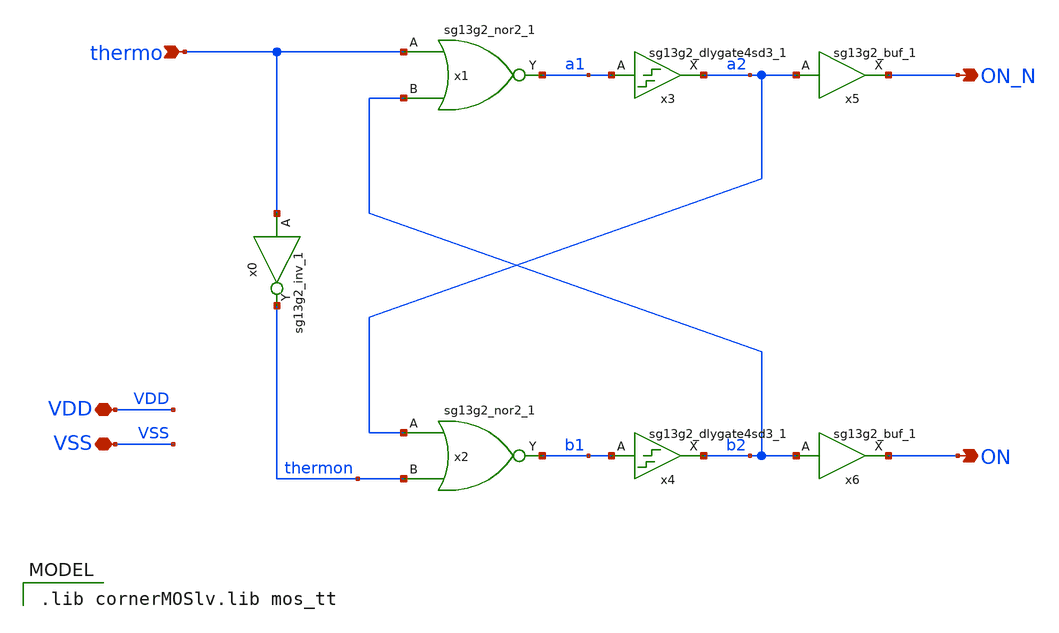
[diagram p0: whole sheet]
** sch_path: analog/non_overlap/xschem/non_overlap.sch
* IHP-GmbH/IHP-Open-PDK/ihp-sg13g2/libs.tech/xschem/sg13g2_stdcells/sg13g2_buf_1.sch:
* Copyright 2023 IHP PDK Authors
* Licensed under the Apache License, Version 2.0 (the "License");
**.subckt non_overlap VSS thermo ON ON_N VDD
*.iopin VSS
*.ipin thermo
*.opin ON
*.opin ON_N
*.iopin VDD
x0 thermon thermo VDD VSS sg13g2_inv_1
x1 a1 thermo b2 VDD VSS sg13g2_nor2_1
x2 b1 a2 thermon VDD VSS sg13g2_nor2_1
x3 a2 a1 VDD VSS sg13g2_dlygate4sd3_1
x4 b2 b1 VDD VSS sg13g2_dlygate4sd3_1
x5 ON_N a2 VDD VSS sg13g2_buf_1
x6 ON b2 VDD VSS sg13g2_buf_1
**** begin user architecture code
 .lib cornerMOSlv.lib mos_tt

**** end user architecture code
**.ends

* expanding   symbol:  sg13g2_stdcells/sg13g2_inv_1.sym # of pins=2
** sym_path: sg13g2_stdcells/sg13g2_inv_1.sym
** sch_path: sg13g2_stdcells/sg13g2_inv_1.sch
.subckt sg13g2_inv_1 Y A VDD VSS
*.opin Y
*.ipin A
*.iopin VDD
*.iopin VSS
XM1 Y A VSS VSS sg13_lv_nmos w=740.00n l=130.00n ng=1 m=1 mm_ok=1
XM2 Y A VDD VDD sg13_lv_pmos w=1.12u l=130.00n ng=1 m=1 mm_ok=1
.ends


* expanding   symbol:  sg13g2_stdcells/sg13g2_nor2_1.sym # of pins=3
** sym_path: sg13g2_stdcells/sg13g2_nor2_1.sym
** sch_path: sg13g2_stdcells/sg13g2_nor2_1.sch
.subckt sg13g2_nor2_1 Y A B VDD VSS
*.opin Y
*.ipin B
*.ipin A
*.iopin VDD
*.iopin VSS
XM1 Y A VSS VSS sg13_lv_nmos w=740.00n l=130.00n ng=1 m=1 mm_ok=1
XM2 Y B VSS VSS sg13_lv_nmos w=740.00n l=130.00n ng=1 m=1 mm_ok=1
XM3 net1 A VDD VDD sg13_lv_pmos w=1.12u l=130.00n ng=1 m=1 mm_ok=1
XM4 Y B net1 VDD sg13_lv_pmos w=1.12u l=130.00n ng=1 m=1 mm_ok=1
.ends


* expanding   symbol:  sg13g2_stdcells/sg13g2_dlygate4sd3_1.sym # of pins=2
** sym_path: sg13g2_stdcells/sg13g2_dlygate4sd3_1.sym
** sch_path: sg13g2_stdcells/sg13g2_dlygate4sd3_1.sch
.subckt sg13g2_dlygate4sd3_1 X A VDD VSS
*.ipin A
*.opin X
*.iopin VDD
*.iopin VSS
XM1 net3 A VSS VSS sg13_lv_nmos w=420.00n l=130.00n ng=1 m=1 mm_ok=1
XM2 net1 net3 VSS VSS sg13_lv_nmos w=420.00n l=500.0n ng=1 m=1 mm_ok=1
XM3 net2 net1 VSS VSS sg13_lv_nmos w=420.00n l=500.0n ng=1 m=1 mm_ok=1
XM4 X net2 VSS VSS sg13_lv_nmos w=740.00n l=130.00n ng=1 m=1 mm_ok=1
XM5 net3 A VDD VDD sg13_lv_pmos w=420.00n l=130.00n ng=1 m=1 mm_ok=1
XM6 net1 net3 VDD VDD sg13_lv_pmos w=1.000u l=500.0n ng=1 m=1 mm_ok=1
XM7 net2 net1 VDD VDD sg13_lv_pmos w=1.000u l=500.0n ng=1 m=1 mm_ok=1
XM8 X net2 VDD VDD sg13_lv_pmos w=1.12u l=130.00n ng=1 m=1 mm_ok=1
.ends


* expanding   symbol:  sg13g2_stdcells/sg13g2_buf_1.sym # of pins=2
** sym_path: sg13g2_stdcells/sg13g2_buf_1.sym
** sch_path: sg13g2_stdcells/sg13g2_buf_1.sch
.subckt sg13g2_buf_1 X A VDD VSS
*.ipin A
*.opin X
*.iopin VDD
*.iopin VSS
XM1 net1 A VSS VSS sg13_lv_nmos w=550.00n l=130.00n ng=1 m=1 mm_ok=1
XM2 X net1 VSS VSS sg13_lv_nmos w=740.00n l=130.00n ng=1 m=1 mm_ok=1
XM3 net1 A VDD VDD sg13_lv_pmos w=840.00n l=130.00n ng=1 m=1 mm_ok=1
XM4 X net1 VDD VDD sg13_lv_pmos w=1.12u l=130.00n ng=1 m=1 mm_ok=1
.ends

.end
